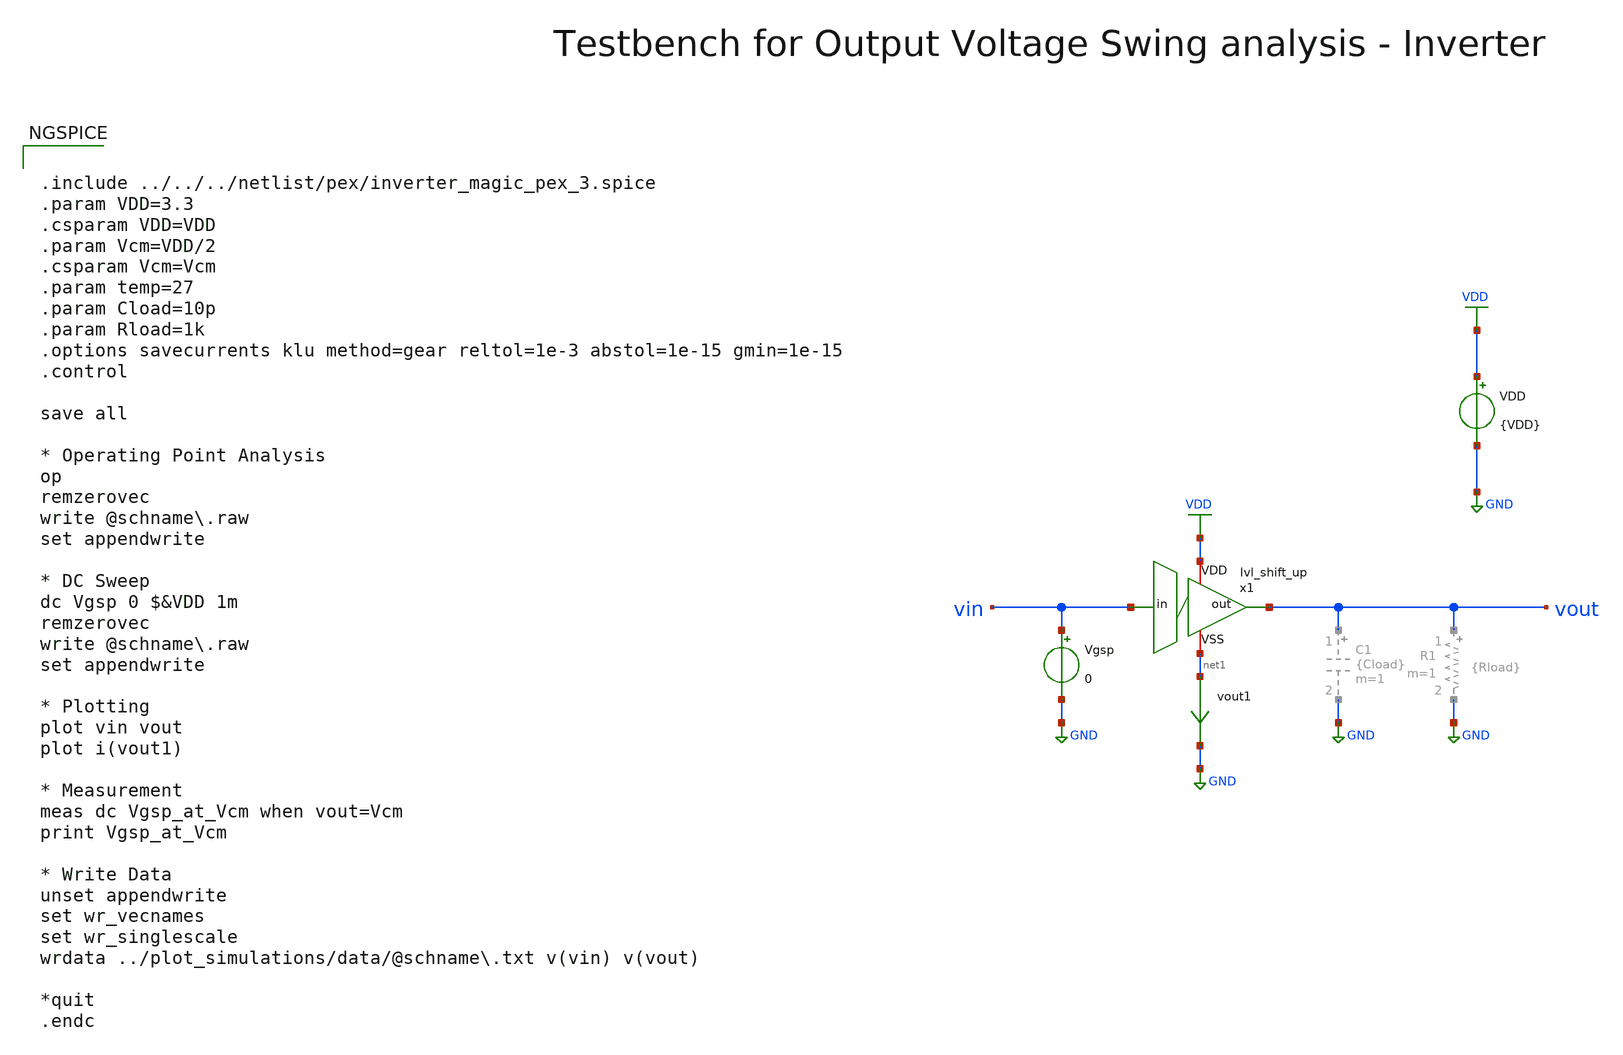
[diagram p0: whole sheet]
** sch_path: macros/heichips26_vcr/macros/switched_capacitor/testbenches/xschem/tb_lvl_shift_up_dc.sch
**.subckt tb_lvl_shift_up_dc
VDD VDD GND {VDD}
Vgsp vin GND 0
vout1 net1 GND 0
.save i(vout1)
x1 VDD vin vout net1 lvl_shift_up
**** begin user architecture code


.include ../../../netlist/pex/inverter_magic_pex_3.spice
.param VDD=3.3
.csparam VDD=VDD
.param Vcm=VDD/2
.csparam Vcm=Vcm
.param temp=27
.param Cload=10p
.param Rload=1k
.options savecurrents klu method=gear reltol=1e-3 abstol=1e-15 gmin=1e-15
.control

save all

* Operating Point Analysis
op
remzerovec
write @schname\.raw
set appendwrite

* DC Sweep
dc Vgsp 0 $&VDD 1m
remzerovec
write @schname\.raw
set appendwrite

* Plotting
plot vin vout
plot i(vout1)

* Measurement
meas dc Vgsp_at_Vcm when vout=Vcm
print Vgsp_at_Vcm

* Write Data
unset appendwrite
set wr_vecnames
set wr_singlescale
wrdata ../plot_simulations/data/@schname\.txt v(vin) v(vout)

*quit
.endc



.lib cornerMOSlv.lib mos_tt
.lib cornerMOShv.lib mos_tt
.lib cornerRES.lib res_typ
.lib cornerDIO.lib dio_tt

**** end user architecture code
**.ends

* expanding   symbol:  lvl_shift_up.sym # of pins=4
** sym_path: macros/heichips26_vcr/macros/switched_capacitor/schematic/xschem/lvl_shift_up.sym
** sch_path: macros/heichips26_vcr/macros/switched_capacitor/schematic/xschem/lvl_shift_up.sch
.subckt lvl_shift_up VDD in out VSS
*.ipin in
*.iopin VDD
*.iopin VSS
*.opin out
XM1 net1 in VSS VSS sg13_hv_nmos w={n_ng*n_w} l={n_l} ng={n_ng} m=1 mm_ok=1
XM2 net1 in VDD VDD sg13_hv_pmos w={p_ng*p_w} l={p_l} ng={n_ng} m=1 mm_ok=1
**** begin user architecture code


.param n_ng = 2
.param n_w = 10u
.param n_l = 0.45u
.param p_ng = 2
.param p_w = 1u
.param p_l = 0.45u


**** end user architecture code
x4 VDD net1 out VSS hv_inverter_6u5
.ends


* expanding   symbol:  hv_inverter_6u5.sym # of pins=4
** sym_path: macros/heichips26_vcr/macros/switched_capacitor/schematic/xschem/hv_inverter_6u5.sym
** sch_path: macros/heichips26_vcr/macros/switched_capacitor/schematic/xschem/hv_inverter_6u5.sch
.subckt hv_inverter_6u5 VDD in out VSS
*.ipin in
*.iopin VDD
*.iopin VSS
*.opin out
XM2 out in VSS VSS sg13_hv_nmos w={n_w} l={n_l} ng={ng} m=1 mm_ok=1
XM3 out in VDD VDD sg13_hv_pmos w={p_w} l={p_l} ng={ng} m=1 mm_ok=1
**** begin user architecture code


.param ng  = 1
.param n_ng = ng
.param n_w = {2u*n_ng}
.param n_l = 0.45u
.param p_ng = ng
.param p_w = {6.5u*p_ng}
.param p_l = 0.4u


**** end user architecture code
.ends

.GLOBAL GND
.GLOBAL VDD
.end
